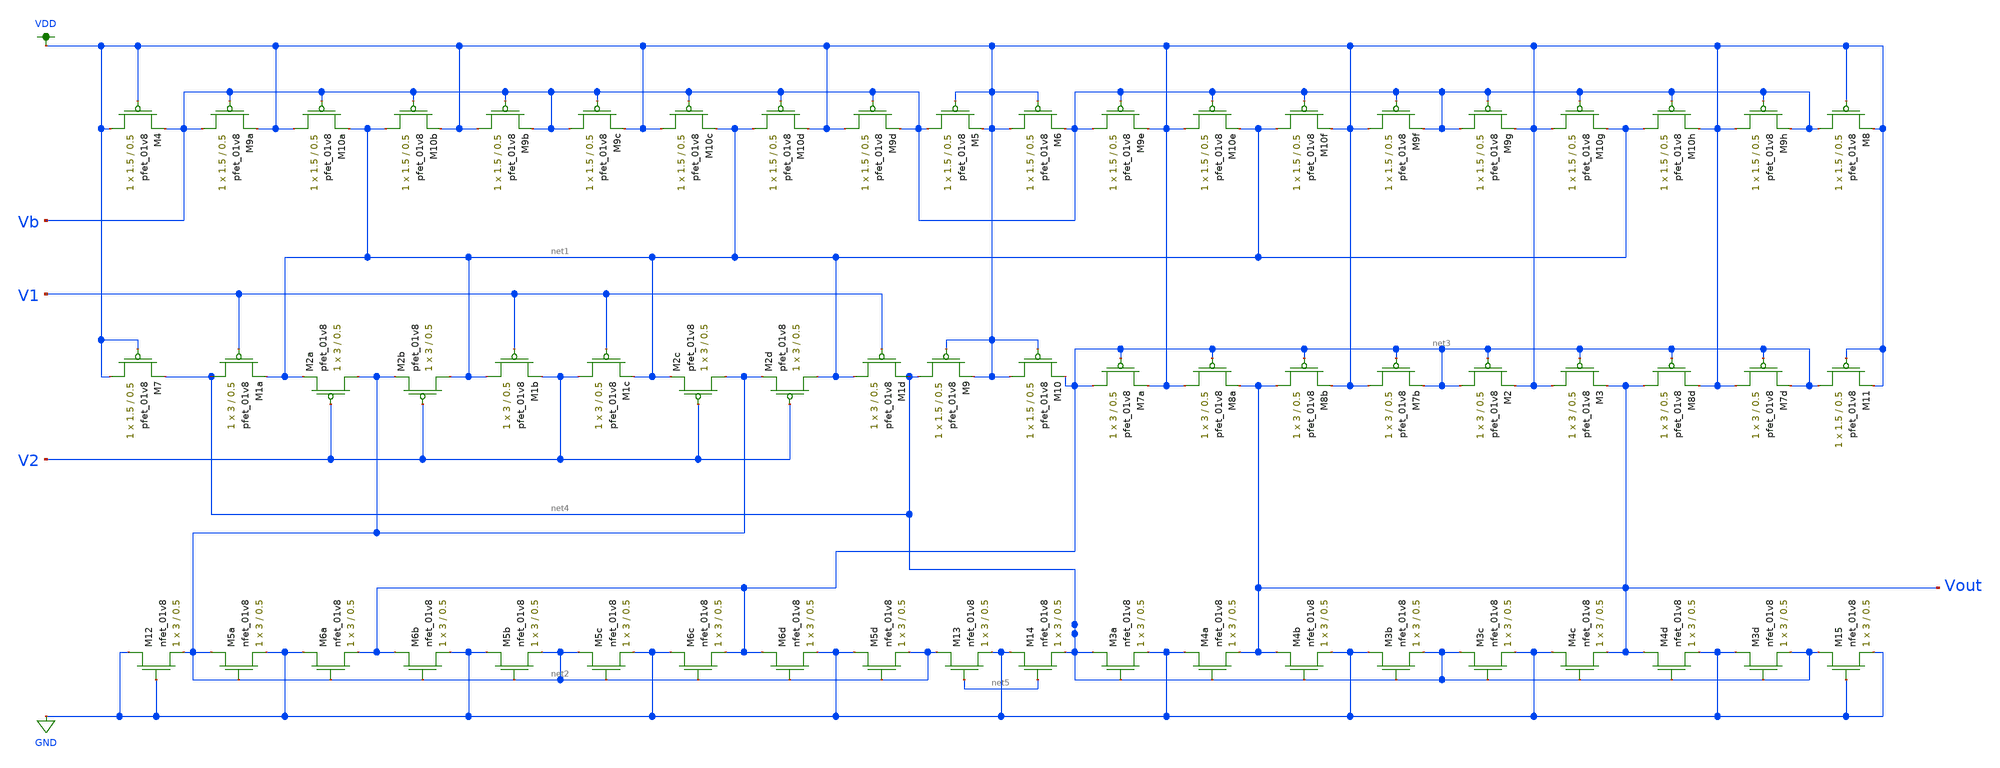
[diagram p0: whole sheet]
** sch_path: Miniproject3/cmdiffamp.sch
**.subckt cmdiffamp
XM1a net4 V1 net1 VDD sky130_fd_pr__pfet_01v8 L=0.5 W=3 nf=1 ad='int((nf+1)/2) * W/nf * 0.29' as='int((nf+2)/2) * W/nf * 0.29'
+ pd='2*int((nf+1)/2) * (W/nf + 0.29)' ps='2*int((nf+2)/2) * (W/nf + 0.29)' nrd='0.29 / W' nrs='0.29 / W'
+ sa=0 sb=0 sd=0 mult=1 m=1
XM2a net2 V2 net1 VDD sky130_fd_pr__pfet_01v8 L=0.5 W=3 nf=1 ad='int((nf+1)/2) * W/nf * 0.29' as='int((nf+2)/2) * W/nf * 0.29'
+ pd='2*int((nf+1)/2) * (W/nf + 0.29)' ps='2*int((nf+2)/2) * (W/nf + 0.29)' nrd='0.29 / W' nrs='0.29 / W'
+ sa=0 sb=0 sd=0 mult=1 m=1
XM2b net1 V2 net2 VDD sky130_fd_pr__pfet_01v8 L=0.5 W=3 nf=1 ad='int((nf+1)/2) * W/nf * 0.29' as='int((nf+2)/2) * W/nf * 0.29'
+ pd='2*int((nf+1)/2) * (W/nf + 0.29)' ps='2*int((nf+2)/2) * (W/nf + 0.29)' nrd='0.29 / W' nrs='0.29 / W'
+ sa=0 sb=0 sd=0 mult=1 m=1
XM1b net1 V1 V2 VDD sky130_fd_pr__pfet_01v8 L=0.5 W=3 nf=1 ad='int((nf+1)/2) * W/nf * 0.29' as='int((nf+2)/2) * W/nf * 0.29'
+ pd='2*int((nf+1)/2) * (W/nf + 0.29)' ps='2*int((nf+2)/2) * (W/nf + 0.29)' nrd='0.29 / W' nrs='0.29 / W'
+ sa=0 sb=0 sd=0 mult=1 m=1
XM1c V2 V1 net1 VDD sky130_fd_pr__pfet_01v8 L=0.5 W=3 nf=1 ad='int((nf+1)/2) * W/nf * 0.29' as='int((nf+2)/2) * W/nf * 0.29'
+ pd='2*int((nf+1)/2) * (W/nf + 0.29)' ps='2*int((nf+2)/2) * (W/nf + 0.29)' nrd='0.29 / W' nrs='0.29 / W'
+ sa=0 sb=0 sd=0 mult=1 m=1
XM2c net2 V2 net1 VDD sky130_fd_pr__pfet_01v8 L=0.5 W=3 nf=1 ad='int((nf+1)/2) * W/nf * 0.29' as='int((nf+2)/2) * W/nf * 0.29'
+ pd='2*int((nf+1)/2) * (W/nf + 0.29)' ps='2*int((nf+2)/2) * (W/nf + 0.29)' nrd='0.29 / W' nrs='0.29 / W'
+ sa=0 sb=0 sd=0 mult=1 m=1
XM2d net1 V2 net2 VDD sky130_fd_pr__pfet_01v8 L=0.5 W=3 nf=1 ad='int((nf+1)/2) * W/nf * 0.29' as='int((nf+2)/2) * W/nf * 0.29'
+ pd='2*int((nf+1)/2) * (W/nf + 0.29)' ps='2*int((nf+2)/2) * (W/nf + 0.29)' nrd='0.29 / W' nrs='0.29 / W'
+ sa=0 sb=0 sd=0 mult=1 m=1
XM1d net1 V1 net4 VDD sky130_fd_pr__pfet_01v8 L=0.5 W=3 nf=1 ad='int((nf+1)/2) * W/nf * 0.29' as='int((nf+2)/2) * W/nf * 0.29'
+ pd='2*int((nf+1)/2) * (W/nf + 0.29)' ps='2*int((nf+2)/2) * (W/nf + 0.29)' nrd='0.29 / W' nrs='0.29 / W'
+ sa=0 sb=0 sd=0 mult=1 m=1
XM5a net2 net2 GND GND sky130_fd_pr__nfet_01v8 L=0.5 W=3 nf=1 ad='int((nf+1)/2) * W/nf * 0.29' as='int((nf+2)/2) * W/nf * 0.29'
+ pd='2*int((nf+1)/2) * (W/nf + 0.29)' ps='2*int((nf+2)/2) * (W/nf + 0.29)' nrd='0.29 / W' nrs='0.29 / W'
+ sa=0 sb=0 sd=0 mult=1 m=1
XM6a GND net2 net3 GND sky130_fd_pr__nfet_01v8 L=0.5 W=3 nf=1 ad='int((nf+1)/2) * W/nf * 0.29' as='int((nf+2)/2) * W/nf * 0.29'
+ pd='2*int((nf+1)/2) * (W/nf + 0.29)' ps='2*int((nf+2)/2) * (W/nf + 0.29)' nrd='0.29 / W' nrs='0.29 / W'
+ sa=0 sb=0 sd=0 mult=1 m=1
XM6b net3 net2 GND GND sky130_fd_pr__nfet_01v8 L=0.5 W=3 nf=1 ad='int((nf+1)/2) * W/nf * 0.29' as='int((nf+2)/2) * W/nf * 0.29'
+ pd='2*int((nf+1)/2) * (W/nf + 0.29)' ps='2*int((nf+2)/2) * (W/nf + 0.29)' nrd='0.29 / W' nrs='0.29 / W'
+ sa=0 sb=0 sd=0 mult=1 m=1
XM5b GND net2 net2 GND sky130_fd_pr__nfet_01v8 L=0.5 W=3 nf=1 ad='int((nf+1)/2) * W/nf * 0.29' as='int((nf+2)/2) * W/nf * 0.29'
+ pd='2*int((nf+1)/2) * (W/nf + 0.29)' ps='2*int((nf+2)/2) * (W/nf + 0.29)' nrd='0.29 / W' nrs='0.29 / W'
+ sa=0 sb=0 sd=0 mult=1 m=1
XM5c net2 net2 GND GND sky130_fd_pr__nfet_01v8 L=0.5 W=3 nf=1 ad='int((nf+1)/2) * W/nf * 0.29' as='int((nf+2)/2) * W/nf * 0.29'
+ pd='2*int((nf+1)/2) * (W/nf + 0.29)' ps='2*int((nf+2)/2) * (W/nf + 0.29)' nrd='0.29 / W' nrs='0.29 / W'
+ sa=0 sb=0 sd=0 mult=1 m=1
XM6c GND net2 net3 GND sky130_fd_pr__nfet_01v8 L=0.5 W=3 nf=1 ad='int((nf+1)/2) * W/nf * 0.29' as='int((nf+2)/2) * W/nf * 0.29'
+ pd='2*int((nf+1)/2) * (W/nf + 0.29)' ps='2*int((nf+2)/2) * (W/nf + 0.29)' nrd='0.29 / W' nrs='0.29 / W'
+ sa=0 sb=0 sd=0 mult=1 m=1
XM6d net3 net2 GND GND sky130_fd_pr__nfet_01v8 L=0.5 W=3 nf=1 ad='int((nf+1)/2) * W/nf * 0.29' as='int((nf+2)/2) * W/nf * 0.29'
+ pd='2*int((nf+1)/2) * (W/nf + 0.29)' ps='2*int((nf+2)/2) * (W/nf + 0.29)' nrd='0.29 / W' nrs='0.29 / W'
+ sa=0 sb=0 sd=0 mult=1 m=1
XM5d GND net2 net2 GND sky130_fd_pr__nfet_01v8 L=0.5 W=3 nf=1 ad='int((nf+1)/2) * W/nf * 0.29' as='int((nf+2)/2) * W/nf * 0.29'
+ pd='2*int((nf+1)/2) * (W/nf + 0.29)' ps='2*int((nf+2)/2) * (W/nf + 0.29)' nrd='0.29 / W' nrs='0.29 / W'
+ sa=0 sb=0 sd=0 mult=1 m=1
XM3a net4 net4 GND GND sky130_fd_pr__nfet_01v8 L=0.5 W=3 nf=1 ad='int((nf+1)/2) * W/nf * 0.29' as='int((nf+2)/2) * W/nf * 0.29'
+ pd='2*int((nf+1)/2) * (W/nf + 0.29)' ps='2*int((nf+2)/2) * (W/nf + 0.29)' nrd='0.29 / W' nrs='0.29 / W'
+ sa=0 sb=0 sd=0 mult=1 m=1
XM4a GND net4 Vout GND sky130_fd_pr__nfet_01v8 L=0.5 W=3 nf=1 ad='int((nf+1)/2) * W/nf * 0.29' as='int((nf+2)/2) * W/nf * 0.29'
+ pd='2*int((nf+1)/2) * (W/nf + 0.29)' ps='2*int((nf+2)/2) * (W/nf + 0.29)' nrd='0.29 / W' nrs='0.29 / W'
+ sa=0 sb=0 sd=0 mult=1 m=1
XM4b Vout net4 GND GND sky130_fd_pr__nfet_01v8 L=0.5 W=3 nf=1 ad='int((nf+1)/2) * W/nf * 0.29' as='int((nf+2)/2) * W/nf * 0.29'
+ pd='2*int((nf+1)/2) * (W/nf + 0.29)' ps='2*int((nf+2)/2) * (W/nf + 0.29)' nrd='0.29 / W' nrs='0.29 / W'
+ sa=0 sb=0 sd=0 mult=1 m=1
XM3b GND net4 net4 GND sky130_fd_pr__nfet_01v8 L=0.5 W=3 nf=1 ad='int((nf+1)/2) * W/nf * 0.29' as='int((nf+2)/2) * W/nf * 0.29'
+ pd='2*int((nf+1)/2) * (W/nf + 0.29)' ps='2*int((nf+2)/2) * (W/nf + 0.29)' nrd='0.29 / W' nrs='0.29 / W'
+ sa=0 sb=0 sd=0 mult=1 m=1
XM3c net4 net4 GND GND sky130_fd_pr__nfet_01v8 L=0.5 W=3 nf=1 ad='int((nf+1)/2) * W/nf * 0.29' as='int((nf+2)/2) * W/nf * 0.29'
+ pd='2*int((nf+1)/2) * (W/nf + 0.29)' ps='2*int((nf+2)/2) * (W/nf + 0.29)' nrd='0.29 / W' nrs='0.29 / W'
+ sa=0 sb=0 sd=0 mult=1 m=1
XM4c GND net4 Vout GND sky130_fd_pr__nfet_01v8 L=0.5 W=3 nf=1 ad='int((nf+1)/2) * W/nf * 0.29' as='int((nf+2)/2) * W/nf * 0.29'
+ pd='2*int((nf+1)/2) * (W/nf + 0.29)' ps='2*int((nf+2)/2) * (W/nf + 0.29)' nrd='0.29 / W' nrs='0.29 / W'
+ sa=0 sb=0 sd=0 mult=1 m=1
XM4d Vout net4 GND GND sky130_fd_pr__nfet_01v8 L=0.5 W=3 nf=1 ad='int((nf+1)/2) * W/nf * 0.29' as='int((nf+2)/2) * W/nf * 0.29'
+ pd='2*int((nf+1)/2) * (W/nf + 0.29)' ps='2*int((nf+2)/2) * (W/nf + 0.29)' nrd='0.29 / W' nrs='0.29 / W'
+ sa=0 sb=0 sd=0 mult=1 m=1
XM3d GND net4 net4 GND sky130_fd_pr__nfet_01v8 L=0.5 W=3 nf=1 ad='int((nf+1)/2) * W/nf * 0.29' as='int((nf+2)/2) * W/nf * 0.29'
+ pd='2*int((nf+1)/2) * (W/nf + 0.29)' ps='2*int((nf+2)/2) * (W/nf + 0.29)' nrd='0.29 / W' nrs='0.29 / W'
+ sa=0 sb=0 sd=0 mult=1 m=1
XM7a net3 net3 VDD VDD sky130_fd_pr__pfet_01v8 L=0.5 W=3 nf=1 ad='int((nf+1)/2) * W/nf * 0.29' as='int((nf+2)/2) * W/nf * 0.29'
+ pd='2*int((nf+1)/2) * (W/nf + 0.29)' ps='2*int((nf+2)/2) * (W/nf + 0.29)' nrd='0.29 / W' nrs='0.29 / W'
+ sa=0 sb=0 sd=0 mult=1 m=1
XM8a VDD net3 Vout VDD sky130_fd_pr__pfet_01v8 L=0.5 W=3 nf=1 ad='int((nf+1)/2) * W/nf * 0.29' as='int((nf+2)/2) * W/nf * 0.29'
+ pd='2*int((nf+1)/2) * (W/nf + 0.29)' ps='2*int((nf+2)/2) * (W/nf + 0.29)' nrd='0.29 / W' nrs='0.29 / W'
+ sa=0 sb=0 sd=0 mult=1 m=1
XM8b Vout net3 VDD VDD sky130_fd_pr__pfet_01v8 L=0.5 W=3 nf=1 ad='int((nf+1)/2) * W/nf * 0.29' as='int((nf+2)/2) * W/nf * 0.29'
+ pd='2*int((nf+1)/2) * (W/nf + 0.29)' ps='2*int((nf+2)/2) * (W/nf + 0.29)' nrd='0.29 / W' nrs='0.29 / W'
+ sa=0 sb=0 sd=0 mult=1 m=1
XM7b VDD net3 net3 VDD sky130_fd_pr__pfet_01v8 L=0.5 W=3 nf=1 ad='int((nf+1)/2) * W/nf * 0.29' as='int((nf+2)/2) * W/nf * 0.29'
+ pd='2*int((nf+1)/2) * (W/nf + 0.29)' ps='2*int((nf+2)/2) * (W/nf + 0.29)' nrd='0.29 / W' nrs='0.29 / W'
+ sa=0 sb=0 sd=0 mult=1 m=1
XM2 net3 net3 VDD VDD sky130_fd_pr__pfet_01v8 L=0.5 W=3 nf=1 ad='int((nf+1)/2) * W/nf * 0.29' as='int((nf+2)/2) * W/nf * 0.29'
+ pd='2*int((nf+1)/2) * (W/nf + 0.29)' ps='2*int((nf+2)/2) * (W/nf + 0.29)' nrd='0.29 / W' nrs='0.29 / W'
+ sa=0 sb=0 sd=0 mult=1 m=1
XM3 VDD net3 Vout VDD sky130_fd_pr__pfet_01v8 L=0.5 W=3 nf=1 ad='int((nf+1)/2) * W/nf * 0.29' as='int((nf+2)/2) * W/nf * 0.29'
+ pd='2*int((nf+1)/2) * (W/nf + 0.29)' ps='2*int((nf+2)/2) * (W/nf + 0.29)' nrd='0.29 / W' nrs='0.29 / W'
+ sa=0 sb=0 sd=0 mult=1 m=1
XM8d Vout net3 VDD VDD sky130_fd_pr__pfet_01v8 L=0.5 W=3 nf=1 ad='int((nf+1)/2) * W/nf * 0.29' as='int((nf+2)/2) * W/nf * 0.29'
+ pd='2*int((nf+1)/2) * (W/nf + 0.29)' ps='2*int((nf+2)/2) * (W/nf + 0.29)' nrd='0.29 / W' nrs='0.29 / W'
+ sa=0 sb=0 sd=0 mult=1 m=1
XM7d VDD net3 net3 VDD sky130_fd_pr__pfet_01v8 L=0.5 W=3 nf=1 ad='int((nf+1)/2) * W/nf * 0.29' as='int((nf+2)/2) * W/nf * 0.29'
+ pd='2*int((nf+1)/2) * (W/nf + 0.29)' ps='2*int((nf+2)/2) * (W/nf + 0.29)' nrd='0.29 / W' nrs='0.29 / W'
+ sa=0 sb=0 sd=0 mult=1 m=1
XM9a Vb Vb VDD VDD sky130_fd_pr__pfet_01v8 L=0.5 W=1.5 nf=1 ad='int((nf+1)/2) * W/nf * 0.29' as='int((nf+2)/2) * W/nf * 0.29'
+ pd='2*int((nf+1)/2) * (W/nf + 0.29)' ps='2*int((nf+2)/2) * (W/nf + 0.29)' nrd='0.29 / W' nrs='0.29 / W'
+ sa=0 sb=0 sd=0 mult=1 m=1
XM10a VDD Vb net1 VDD sky130_fd_pr__pfet_01v8 L=0.5 W=1.5 nf=1 ad='int((nf+1)/2) * W/nf * 0.29' as='int((nf+2)/2) * W/nf * 0.29'
+ pd='2*int((nf+1)/2) * (W/nf + 0.29)' ps='2*int((nf+2)/2) * (W/nf + 0.29)' nrd='0.29 / W' nrs='0.29 / W'
+ sa=0 sb=0 sd=0 mult=1 m=1
XM10b net1 Vb VDD VDD sky130_fd_pr__pfet_01v8 L=0.5 W=1.5 nf=1 ad='int((nf+1)/2) * W/nf * 0.29' as='int((nf+2)/2) * W/nf * 0.29'
+ pd='2*int((nf+1)/2) * (W/nf + 0.29)' ps='2*int((nf+2)/2) * (W/nf + 0.29)' nrd='0.29 / W' nrs='0.29 / W'
+ sa=0 sb=0 sd=0 mult=1 m=1
XM9b VDD Vb Vb VDD sky130_fd_pr__pfet_01v8 L=0.5 W=1.5 nf=1 ad='int((nf+1)/2) * W/nf * 0.29' as='int((nf+2)/2) * W/nf * 0.29'
+ pd='2*int((nf+1)/2) * (W/nf + 0.29)' ps='2*int((nf+2)/2) * (W/nf + 0.29)' nrd='0.29 / W' nrs='0.29 / W'
+ sa=0 sb=0 sd=0 mult=1 m=1
XM9c Vb Vb VDD VDD sky130_fd_pr__pfet_01v8 L=0.5 W=1.5 nf=1 ad='int((nf+1)/2) * W/nf * 0.29' as='int((nf+2)/2) * W/nf * 0.29'
+ pd='2*int((nf+1)/2) * (W/nf + 0.29)' ps='2*int((nf+2)/2) * (W/nf + 0.29)' nrd='0.29 / W' nrs='0.29 / W'
+ sa=0 sb=0 sd=0 mult=1 m=1
XM10c VDD Vb net1 VDD sky130_fd_pr__pfet_01v8 L=0.5 W=1.5 nf=1 ad='int((nf+1)/2) * W/nf * 0.29' as='int((nf+2)/2) * W/nf * 0.29'
+ pd='2*int((nf+1)/2) * (W/nf + 0.29)' ps='2*int((nf+2)/2) * (W/nf + 0.29)' nrd='0.29 / W' nrs='0.29 / W'
+ sa=0 sb=0 sd=0 mult=1 m=1
XM10d net1 Vb VDD VDD sky130_fd_pr__pfet_01v8 L=0.5 W=1.5 nf=1 ad='int((nf+1)/2) * W/nf * 0.29' as='int((nf+2)/2) * W/nf * 0.29'
+ pd='2*int((nf+1)/2) * (W/nf + 0.29)' ps='2*int((nf+2)/2) * (W/nf + 0.29)' nrd='0.29 / W' nrs='0.29 / W'
+ sa=0 sb=0 sd=0 mult=1 m=1
XM9d VDD Vb Vb VDD sky130_fd_pr__pfet_01v8 L=0.5 W=1.5 nf=1 ad='int((nf+1)/2) * W/nf * 0.29' as='int((nf+2)/2) * W/nf * 0.29'
+ pd='2*int((nf+1)/2) * (W/nf + 0.29)' ps='2*int((nf+2)/2) * (W/nf + 0.29)' nrd='0.29 / W' nrs='0.29 / W'
+ sa=0 sb=0 sd=0 mult=1 m=1
XM9e Vb Vb VDD VDD sky130_fd_pr__pfet_01v8 L=0.5 W=1.5 nf=1 ad='int((nf+1)/2) * W/nf * 0.29' as='int((nf+2)/2) * W/nf * 0.29'
+ pd='2*int((nf+1)/2) * (W/nf + 0.29)' ps='2*int((nf+2)/2) * (W/nf + 0.29)' nrd='0.29 / W' nrs='0.29 / W'
+ sa=0 sb=0 sd=0 mult=1 m=1
XM10e VDD Vb net1 VDD sky130_fd_pr__pfet_01v8 L=0.5 W=1.5 nf=1 ad='int((nf+1)/2) * W/nf * 0.29' as='int((nf+2)/2) * W/nf * 0.29'
+ pd='2*int((nf+1)/2) * (W/nf + 0.29)' ps='2*int((nf+2)/2) * (W/nf + 0.29)' nrd='0.29 / W' nrs='0.29 / W'
+ sa=0 sb=0 sd=0 mult=1 m=1
XM10f net1 Vb VDD VDD sky130_fd_pr__pfet_01v8 L=0.5 W=1.5 nf=1 ad='int((nf+1)/2) * W/nf * 0.29' as='int((nf+2)/2) * W/nf * 0.29'
+ pd='2*int((nf+1)/2) * (W/nf + 0.29)' ps='2*int((nf+2)/2) * (W/nf + 0.29)' nrd='0.29 / W' nrs='0.29 / W'
+ sa=0 sb=0 sd=0 mult=1 m=1
XM9f VDD Vb Vb VDD sky130_fd_pr__pfet_01v8 L=0.5 W=1.5 nf=1 ad='int((nf+1)/2) * W/nf * 0.29' as='int((nf+2)/2) * W/nf * 0.29'
+ pd='2*int((nf+1)/2) * (W/nf + 0.29)' ps='2*int((nf+2)/2) * (W/nf + 0.29)' nrd='0.29 / W' nrs='0.29 / W'
+ sa=0 sb=0 sd=0 mult=1 m=1
XM9g Vb Vb VDD VDD sky130_fd_pr__pfet_01v8 L=0.5 W=1.5 nf=1 ad='int((nf+1)/2) * W/nf * 0.29' as='int((nf+2)/2) * W/nf * 0.29'
+ pd='2*int((nf+1)/2) * (W/nf + 0.29)' ps='2*int((nf+2)/2) * (W/nf + 0.29)' nrd='0.29 / W' nrs='0.29 / W'
+ sa=0 sb=0 sd=0 mult=1 m=1
XM10g VDD Vb net1 VDD sky130_fd_pr__pfet_01v8 L=0.5 W=1.5 nf=1 ad='int((nf+1)/2) * W/nf * 0.29' as='int((nf+2)/2) * W/nf * 0.29'
+ pd='2*int((nf+1)/2) * (W/nf + 0.29)' ps='2*int((nf+2)/2) * (W/nf + 0.29)' nrd='0.29 / W' nrs='0.29 / W'
+ sa=0 sb=0 sd=0 mult=1 m=1
XM10h net1 Vb VDD VDD sky130_fd_pr__pfet_01v8 L=0.5 W=1.5 nf=1 ad='int((nf+1)/2) * W/nf * 0.29' as='int((nf+2)/2) * W/nf * 0.29'
+ pd='2*int((nf+1)/2) * (W/nf + 0.29)' ps='2*int((nf+2)/2) * (W/nf + 0.29)' nrd='0.29 / W' nrs='0.29 / W'
+ sa=0 sb=0 sd=0 mult=1 m=1
XM9h VDD Vb Vb VDD sky130_fd_pr__pfet_01v8 L=0.5 W=1.5 nf=1 ad='int((nf+1)/2) * W/nf * 0.29' as='int((nf+2)/2) * W/nf * 0.29'
+ pd='2*int((nf+1)/2) * (W/nf + 0.29)' ps='2*int((nf+2)/2) * (W/nf + 0.29)' nrd='0.29 / W' nrs='0.29 / W'
+ sa=0 sb=0 sd=0 mult=1 m=1
XM4 VDD VDD Vb VDD sky130_fd_pr__pfet_01v8 L=0.5 W=1.5 nf=1 ad='int((nf+1)/2) * W/nf * 0.29' as='int((nf+2)/2) * W/nf * 0.29'
+ pd='2*int((nf+1)/2) * (W/nf + 0.29)' ps='2*int((nf+2)/2) * (W/nf + 0.29)' nrd='0.29 / W' nrs='0.29 / W'
+ sa=0 sb=0 sd=0 mult=1 m=1
XM5 Vb VDD VDD VDD sky130_fd_pr__pfet_01v8 L=0.5 W=1.5 nf=1 ad='int((nf+1)/2) * W/nf * 0.29' as='int((nf+2)/2) * W/nf * 0.29'
+ pd='2*int((nf+1)/2) * (W/nf + 0.29)' ps='2*int((nf+2)/2) * (W/nf + 0.29)' nrd='0.29 / W' nrs='0.29 / W'
+ sa=0 sb=0 sd=0 mult=1 m=1
XM6 VDD VDD Vb VDD sky130_fd_pr__pfet_01v8 L=0.5 W=1.5 nf=1 ad='int((nf+1)/2) * W/nf * 0.29' as='int((nf+2)/2) * W/nf * 0.29'
+ pd='2*int((nf+1)/2) * (W/nf + 0.29)' ps='2*int((nf+2)/2) * (W/nf + 0.29)' nrd='0.29 / W' nrs='0.29 / W'
+ sa=0 sb=0 sd=0 mult=1 m=1
XM8 Vb VDD VDD VDD sky130_fd_pr__pfet_01v8 L=0.5 W=1.5 nf=1 ad='int((nf+1)/2) * W/nf * 0.29' as='int((nf+2)/2) * W/nf * 0.29'
+ pd='2*int((nf+1)/2) * (W/nf + 0.29)' ps='2*int((nf+2)/2) * (W/nf + 0.29)' nrd='0.29 / W' nrs='0.29 / W'
+ sa=0 sb=0 sd=0 mult=1 m=1
XM7 VDD VDD net4 VDD sky130_fd_pr__pfet_01v8 L=0.5 W=1.5 nf=1 ad='int((nf+1)/2) * W/nf * 0.29' as='int((nf+2)/2) * W/nf * 0.29'
+ pd='2*int((nf+1)/2) * (W/nf + 0.29)' ps='2*int((nf+2)/2) * (W/nf + 0.29)' nrd='0.29 / W' nrs='0.29 / W'
+ sa=0 sb=0 sd=0 mult=1 m=1
XM9 net4 VDD VDD VDD sky130_fd_pr__pfet_01v8 L=0.5 W=1.5 nf=1 ad='int((nf+1)/2) * W/nf * 0.29' as='int((nf+2)/2) * W/nf * 0.29'
+ pd='2*int((nf+1)/2) * (W/nf + 0.29)' ps='2*int((nf+2)/2) * (W/nf + 0.29)' nrd='0.29 / W' nrs='0.29 / W'
+ sa=0 sb=0 sd=0 mult=1 m=1
XM10 VDD VDD net3 VDD sky130_fd_pr__pfet_01v8 L=0.5 W=1.5 nf=1 ad='int((nf+1)/2) * W/nf * 0.29' as='int((nf+2)/2) * W/nf * 0.29'
+ pd='2*int((nf+1)/2) * (W/nf + 0.29)' ps='2*int((nf+2)/2) * (W/nf + 0.29)' nrd='0.29 / W' nrs='0.29 / W'
+ sa=0 sb=0 sd=0 mult=1 m=1
XM11 net3 VDD VDD VDD sky130_fd_pr__pfet_01v8 L=0.5 W=1.5 nf=1 ad='int((nf+1)/2) * W/nf * 0.29' as='int((nf+2)/2) * W/nf * 0.29'
+ pd='2*int((nf+1)/2) * (W/nf + 0.29)' ps='2*int((nf+2)/2) * (W/nf + 0.29)' nrd='0.29 / W' nrs='0.29 / W'
+ sa=0 sb=0 sd=0 mult=1 m=1
XM12 GND GND net2 GND sky130_fd_pr__nfet_01v8 L=0.5 W=3 nf=1 ad='int((nf+1)/2) * W/nf * 0.29' as='int((nf+2)/2) * W/nf * 0.29'
+ pd='2*int((nf+1)/2) * (W/nf + 0.29)' ps='2*int((nf+2)/2) * (W/nf + 0.29)' nrd='0.29 / W' nrs='0.29 / W'
+ sa=0 sb=0 sd=0 mult=1 m=1
XM13 net2 net5 GND GND sky130_fd_pr__nfet_01v8 L=0.5 W=3 nf=1 ad='int((nf+1)/2) * W/nf * 0.29' as='int((nf+2)/2) * W/nf * 0.29'
+ pd='2*int((nf+1)/2) * (W/nf + 0.29)' ps='2*int((nf+2)/2) * (W/nf + 0.29)' nrd='0.29 / W' nrs='0.29 / W'
+ sa=0 sb=0 sd=0 mult=1 m=1
XM14 GND net5 net4 GND sky130_fd_pr__nfet_01v8 L=0.5 W=3 nf=1 ad='int((nf+1)/2) * W/nf * 0.29' as='int((nf+2)/2) * W/nf * 0.29'
+ pd='2*int((nf+1)/2) * (W/nf + 0.29)' ps='2*int((nf+2)/2) * (W/nf + 0.29)' nrd='0.29 / W' nrs='0.29 / W'
+ sa=0 sb=0 sd=0 mult=1 m=1
XM15 net4 GND GND GND sky130_fd_pr__nfet_01v8 L=0.5 W=3 nf=1 ad='int((nf+1)/2) * W/nf * 0.29' as='int((nf+2)/2) * W/nf * 0.29'
+ pd='2*int((nf+1)/2) * (W/nf + 0.29)' ps='2*int((nf+2)/2) * (W/nf + 0.29)' nrd='0.29 / W' nrs='0.29 / W'
+ sa=0 sb=0 sd=0 mult=1 m=1
**.ends
.GLOBAL GND
.GLOBAL VDD
.end
